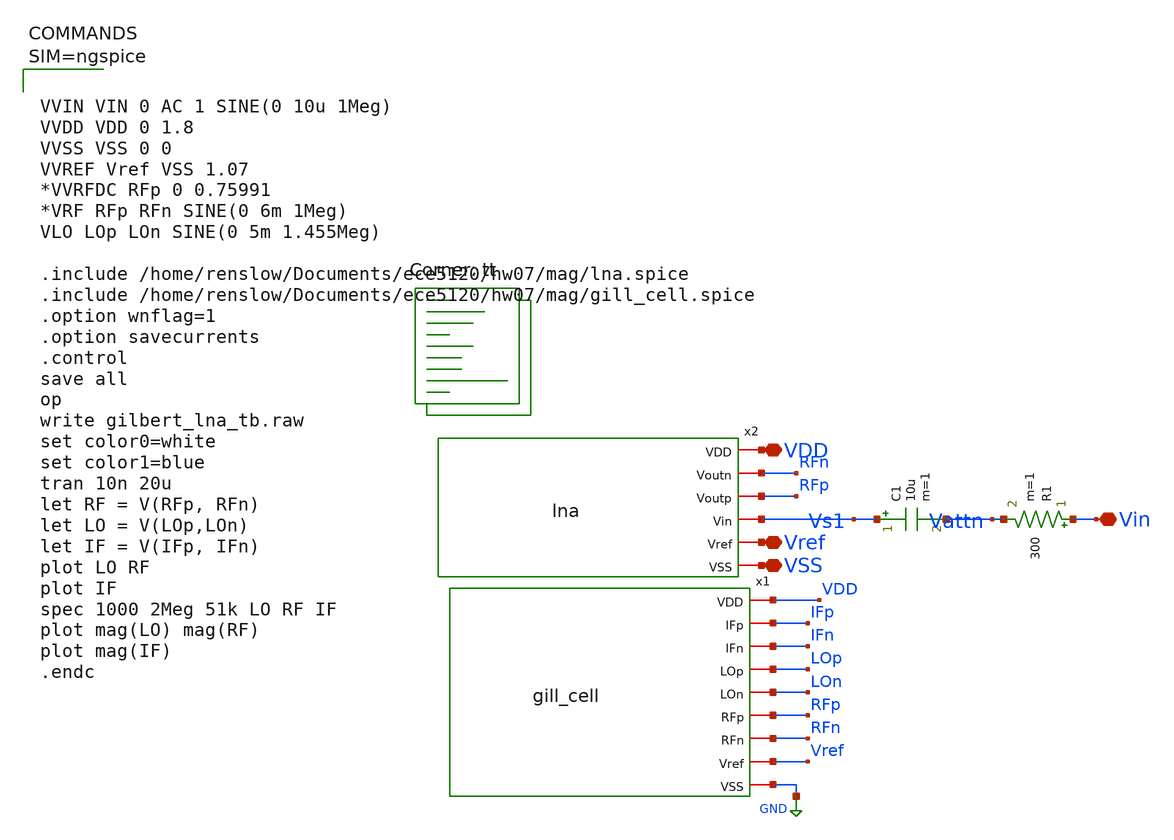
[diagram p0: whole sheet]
** sch_path: hw07/mag/gilbert_lna_tb.sch
**.subckt gilbert_lna_tb VDD Vin Vref VSS
*.iopin VDD
*.iopin Vin
*.iopin Vref
*.iopin VSS
x1 VDD IFp IFn LOp LOn RFp RFn Vref GND gill_cell
C1 Vs1 Vattn 10u m=1
R1 Vin Vattn 300 m=1
x2 VDD RFn RFp Vs1 Vref VSS lna
**** begin user architecture code



VVIN VIN 0 AC 1 SINE(0 10u 1Meg)
VVDD VDD 0 1.8
VVSS VSS 0 0
VVREF Vref VSS 1.07
*VVRFDC RFp 0 0.75991
*VRF RFp RFn SINE(0 6m 1Meg)
VLO LOp LOn SINE(0 5m 1.455Meg)

.include /home/renslow/Documents/ece5120/hw07/mag/lna.spice
.include /home/renslow/Documents/ece5120/hw07/mag/gill_cell.spice
.option wnflag=1
.option savecurrents
.control
save all
op
write gilbert_lna_tb.raw
set color0=white
set color1=blue
tran 10n 20u
let RF = V(RFp, RFn)
let LO = V(LOp,LOn)
let IF = V(IFp, IFn)
plot LO RF
plot IF
spec 1000 2Meg 51k LO RF IF
plot mag(LO) mag(RF)
plot mag(IF)
.endc



.lib $::SKYWATER_MODELS/sky130.lib.spice tt
**** end user architecture code
**.ends
.GLOBAL GND
.end
